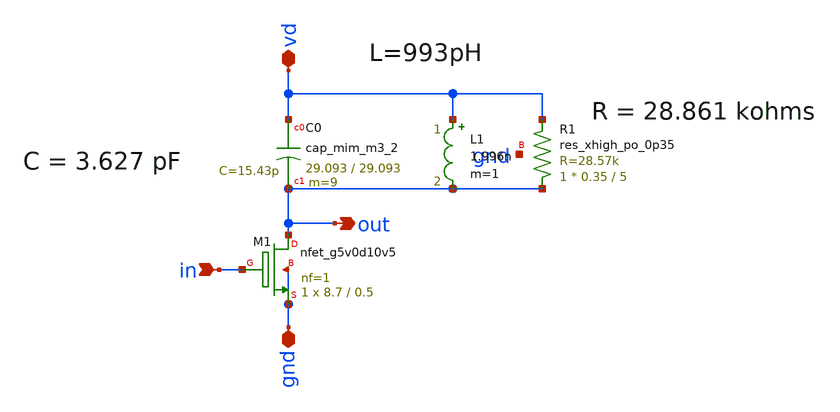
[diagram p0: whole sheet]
** sch_path: xschem-915MHz/ask-915M-0.sch
**.subckt ask-915M-0 gnd in out vd
*.iopin gnd
*.ipin in
*.opin out
*.iopin vd
XC0 vd out sky130_fd_pr__cap_mim_m3_2 W=29.093 L=29.093 MF=9 m=9
XM1 out in gnd gnd sky130_fd_pr__nfet_g5v0d10v5 L=0.5 W=8.7 nf=1 ad='int((nf+1)/2) * W/nf * 0.29' as='int((nf+2)/2) * W/nf * 0.29'
+ pd='2*int((nf+1)/2) * (W/nf + 0.29)' ps='2*int((nf+2)/2) * (W/nf + 0.29)' nrd='0.29 / W' nrs='0.29 / W'
+ sa=0 sb=0 sd=0 mult=1 m=1
XR1 out vd gnd sky130_fd_pr__res_xhigh_po_0p35 L=5 mult=1 m=1
L1 vd out 1.996n m=1
**.ends
.end
